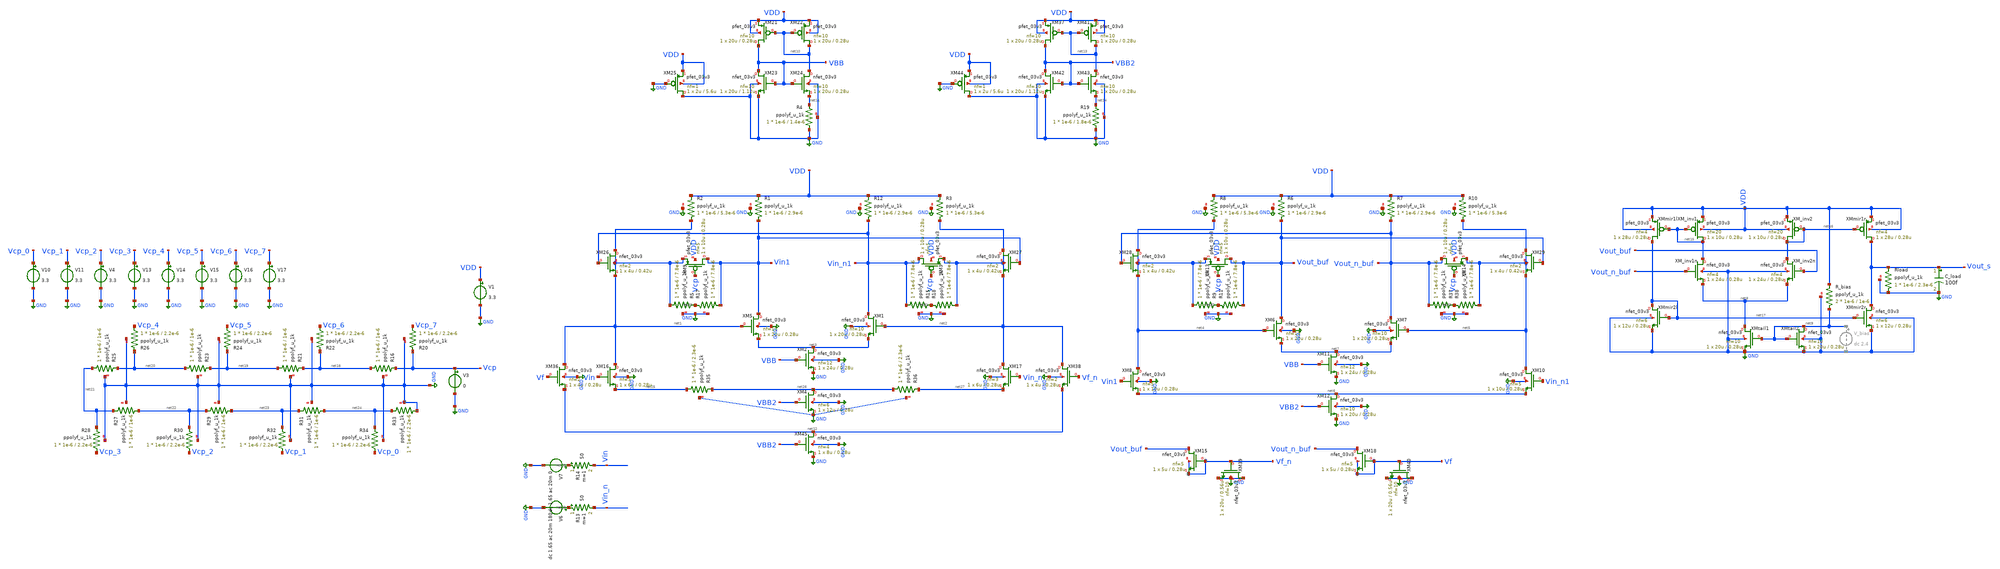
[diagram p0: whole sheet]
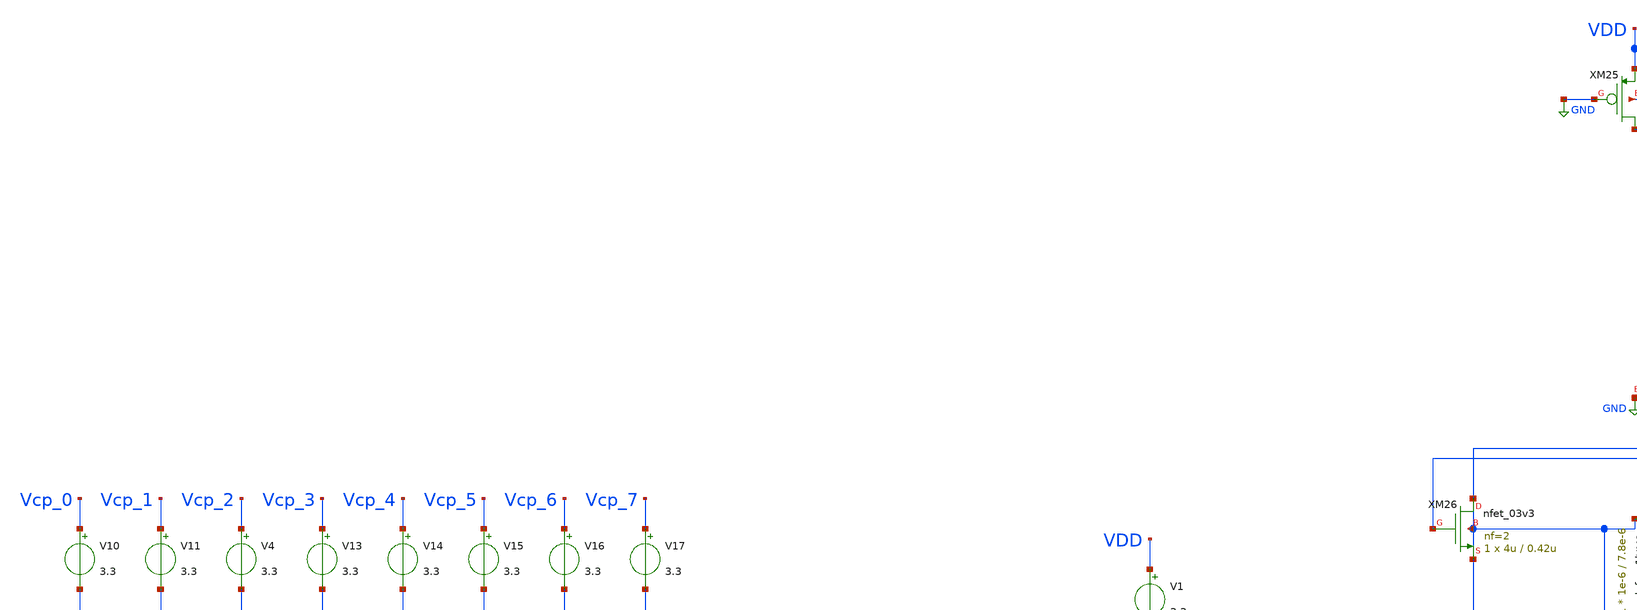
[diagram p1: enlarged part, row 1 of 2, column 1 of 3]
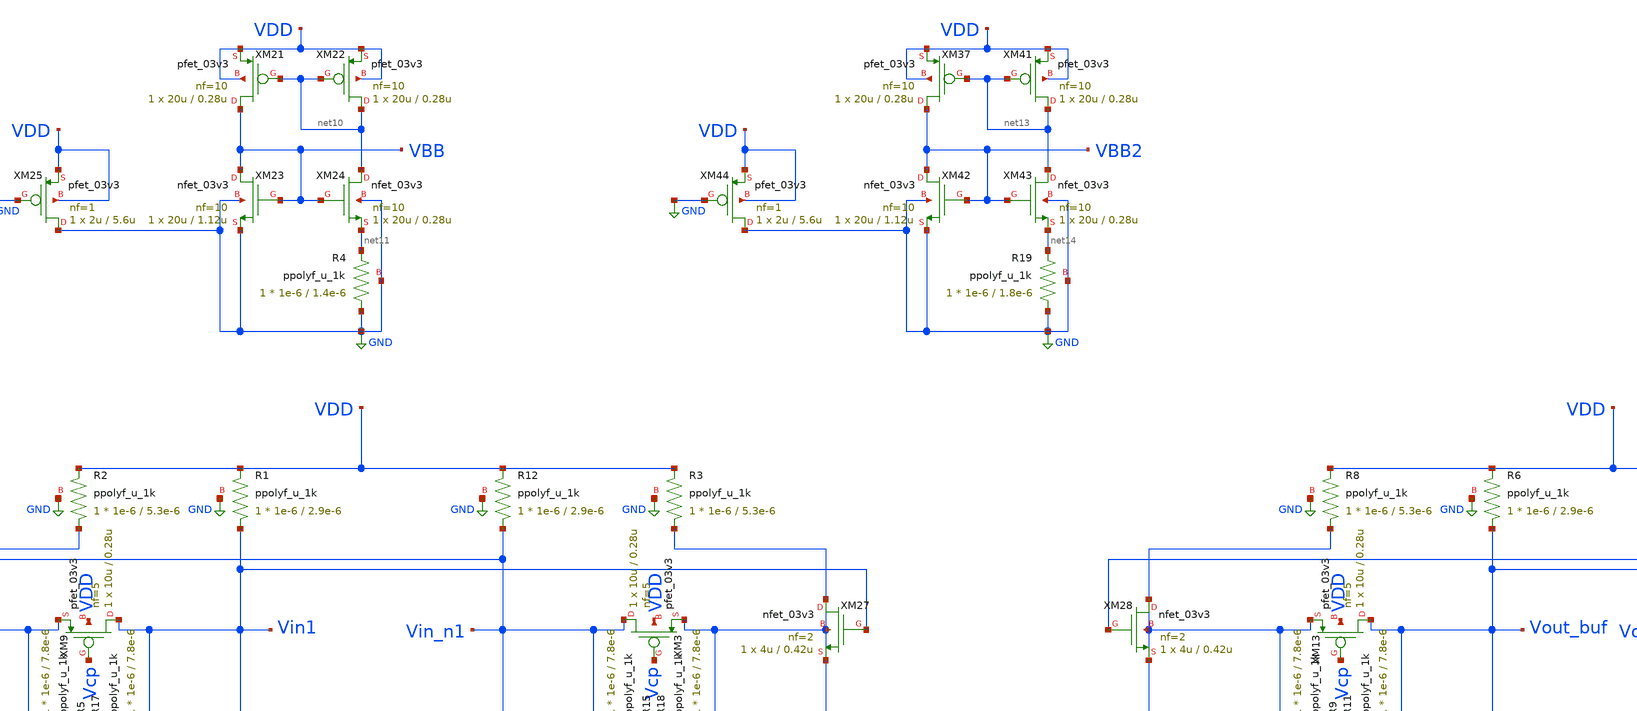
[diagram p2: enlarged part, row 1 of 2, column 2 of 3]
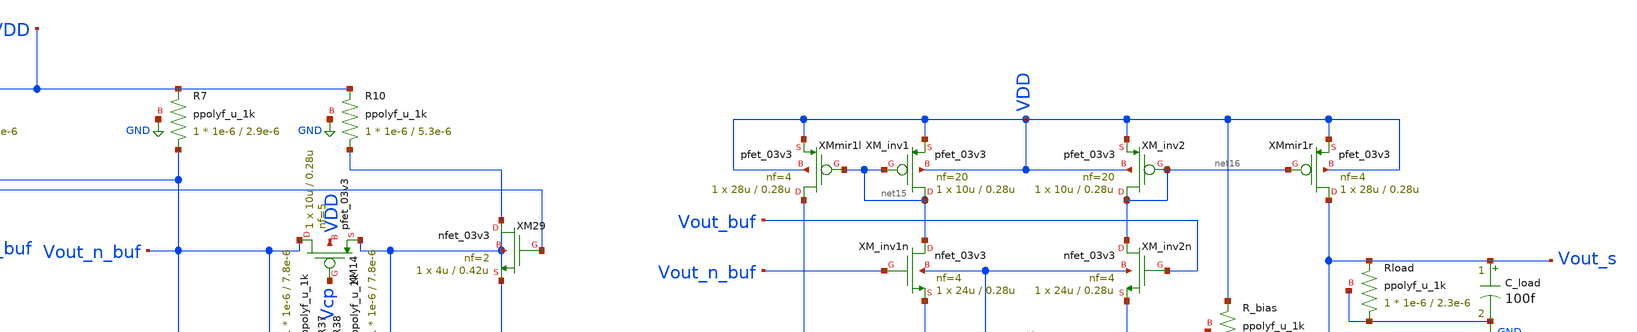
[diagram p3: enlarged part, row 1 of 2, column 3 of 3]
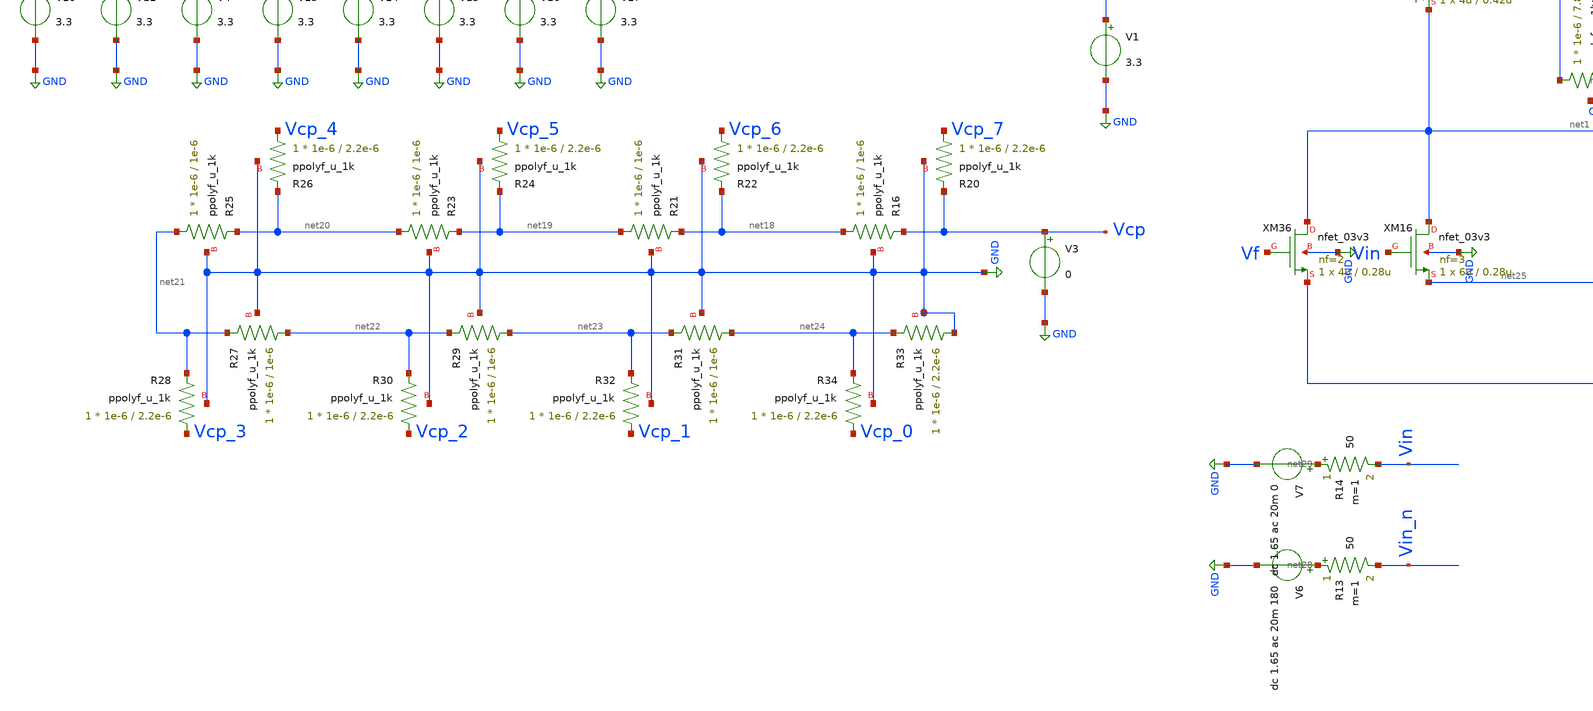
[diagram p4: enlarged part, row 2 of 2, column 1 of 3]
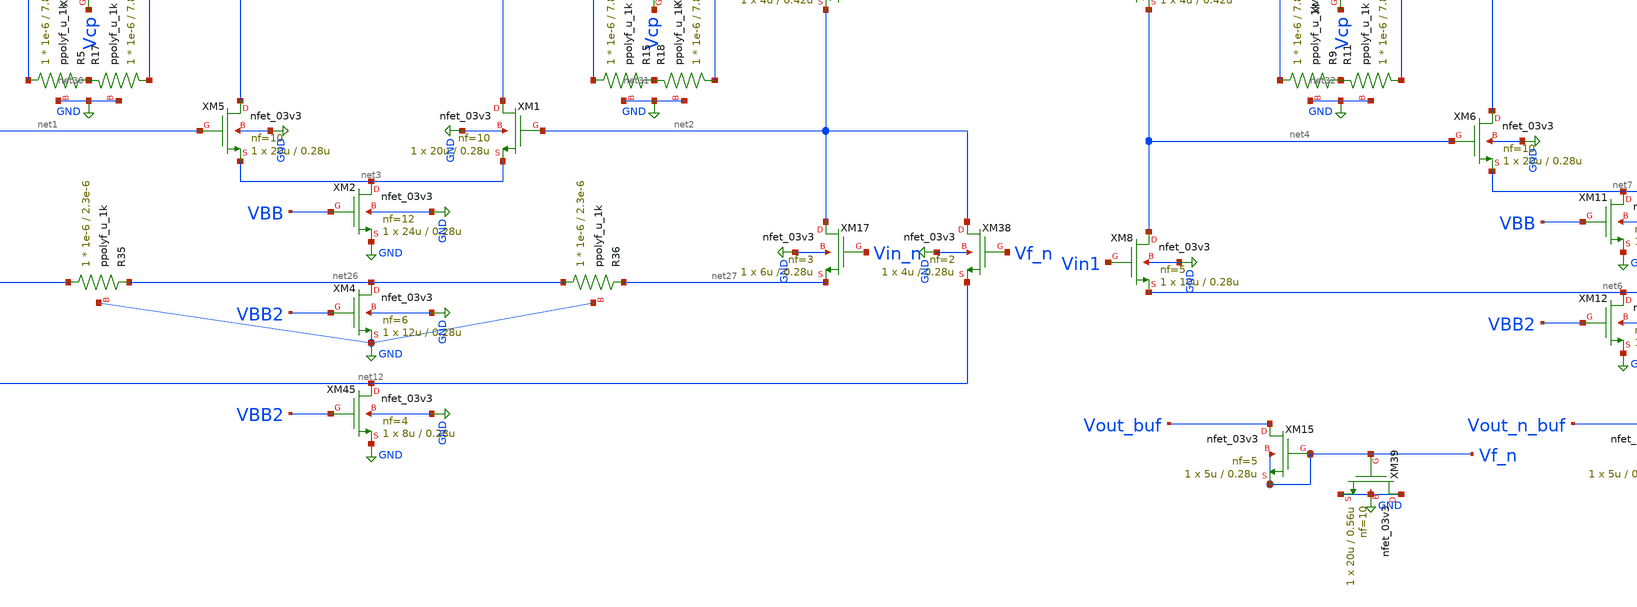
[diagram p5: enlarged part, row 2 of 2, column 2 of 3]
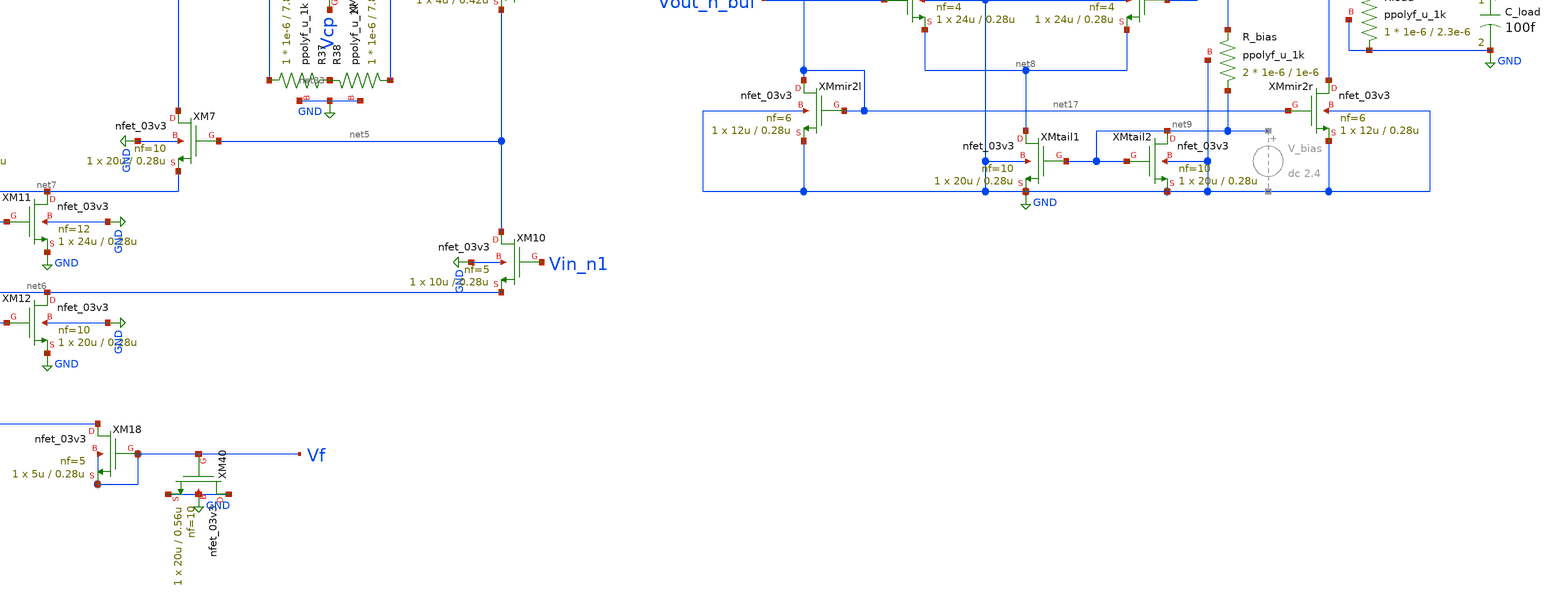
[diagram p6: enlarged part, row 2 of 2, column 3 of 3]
** sch_path: blocks/vga/vga.sch
**.subckt vga
V1 VDD GND 3.3
V6 net28 GND dc 1.65 ac 20m 180
XM5 Vin1 net1 net3 GND nfet_03v3 L=0.28u W=20u nf=10 ad='int((nf+1)/2) * W/nf * 0.18u' as='int((nf+2)/2) * W/nf * 0.18u'
+ pd='2*int((nf+1)/2) * (W/nf + 0.18u)' ps='2*int((nf+2)/2) * (W/nf + 0.18u)' nrd='0.18u / W' nrs='0.18u / W'
+ sa=0 sb=0 sd=0 m=1
XM1 Vin_n1 net2 net3 GND nfet_03v3 L=0.28u W=20u nf=10 ad='int((nf+1)/2) * W/nf * 0.18u' as='int((nf+2)/2) * W/nf * 0.18u'
+ pd='2*int((nf+1)/2) * (W/nf + 0.18u)' ps='2*int((nf+2)/2) * (W/nf + 0.18u)' nrd='0.18u / W' nrs='0.18u / W'
+ sa=0 sb=0 sd=0 m=1
XM16 net1 Vin net25 GND nfet_03v3 L=0.28u W=6u nf=3 ad='int((nf+1)/2) * W/nf * 0.18u' as='int((nf+2)/2) * W/nf * 0.18u'
+ pd='2*int((nf+1)/2) * (W/nf + 0.18u)' ps='2*int((nf+2)/2) * (W/nf + 0.18u)' nrd='0.18u / W' nrs='0.18u / W'
+ sa=0 sb=0 sd=0 m=1
XM17 net2 Vin_n net27 GND nfet_03v3 L=0.28u W=6u nf=3 ad='int((nf+1)/2) * W/nf * 0.18u' as='int((nf+2)/2) * W/nf * 0.18u'
+ pd='2*int((nf+1)/2) * (W/nf + 0.18u)' ps='2*int((nf+2)/2) * (W/nf + 0.18u)' nrd='0.18u / W' nrs='0.18u / W'
+ sa=0 sb=0 sd=0 m=1
XM2 net3 VBB GND GND nfet_03v3 L=0.28u W=24u nf=12 ad='int((nf+1)/2) * W/nf * 0.18u' as='int((nf+2)/2) * W/nf * 0.18u'
+ pd='2*int((nf+1)/2) * (W/nf + 0.18u)' ps='2*int((nf+2)/2) * (W/nf + 0.18u)' nrd='0.18u / W' nrs='0.18u / W'
+ sa=0 sb=0 sd=0 m=1
XM4 net26 VBB2 GND GND nfet_03v3 L=0.28u W=12u nf=6 ad='int((nf+1)/2) * W/nf * 0.18u' as='int((nf+2)/2) * W/nf * 0.18u'
+ pd='2*int((nf+1)/2) * (W/nf + 0.18u)' ps='2*int((nf+2)/2) * (W/nf + 0.18u)' nrd='0.18u / W' nrs='0.18u / W'
+ sa=0 sb=0 sd=0 m=1
XM9 Vin1 Vcp net1 VDD pfet_03v3 L=0.28u W=10u nf=5 ad='int((nf+1)/2) * W/nf * 0.18u' as='int((nf+2)/2) * W/nf * 0.18u'
+ pd='2*int((nf+1)/2) * (W/nf + 0.18u)' ps='2*int((nf+2)/2) * (W/nf + 0.18u)' nrd='0.18u / W' nrs='0.18u / W'
+ sa=0 sb=0 sd=0 m=1
XM6 Vout_buf net4 net7 GND nfet_03v3 L=0.28u W=20u nf=10 ad='int((nf+1)/2) * W/nf * 0.18u' as='int((nf+2)/2) * W/nf * 0.18u'
+ pd='2*int((nf+1)/2) * (W/nf + 0.18u)' ps='2*int((nf+2)/2) * (W/nf + 0.18u)' nrd='0.18u / W' nrs='0.18u / W'
+ sa=0 sb=0 sd=0 m=1
XM7 Vout_n_buf net5 net7 GND nfet_03v3 L=0.28u W=20u nf=10 ad='int((nf+1)/2) * W/nf * 0.18u' as='int((nf+2)/2) * W/nf * 0.18u'
+ pd='2*int((nf+1)/2) * (W/nf + 0.18u)' ps='2*int((nf+2)/2) * (W/nf + 0.18u)' nrd='0.18u / W' nrs='0.18u / W'
+ sa=0 sb=0 sd=0 m=1
XM8 net4 Vin1 net6 GND nfet_03v3 L=0.28u W=10u nf=5 ad='int((nf+1)/2) * W/nf * 0.18u' as='int((nf+2)/2) * W/nf * 0.18u'
+ pd='2*int((nf+1)/2) * (W/nf + 0.18u)' ps='2*int((nf+2)/2) * (W/nf + 0.18u)' nrd='0.18u / W' nrs='0.18u / W'
+ sa=0 sb=0 sd=0 m=1
XM10 net5 Vin_n1 net6 GND nfet_03v3 L=0.28u W=10u nf=5 ad='int((nf+1)/2) * W/nf * 0.18u' as='int((nf+2)/2) * W/nf * 0.18u'
+ pd='2*int((nf+1)/2) * (W/nf + 0.18u)' ps='2*int((nf+2)/2) * (W/nf + 0.18u)' nrd='0.18u / W' nrs='0.18u / W'
+ sa=0 sb=0 sd=0 m=1
XM11 net7 VBB GND GND nfet_03v3 L=0.28u W=24u nf=12 ad='int((nf+1)/2) * W/nf * 0.18u' as='int((nf+2)/2) * W/nf * 0.18u'
+ pd='2*int((nf+1)/2) * (W/nf + 0.18u)' ps='2*int((nf+2)/2) * (W/nf + 0.18u)' nrd='0.18u / W' nrs='0.18u / W'
+ sa=0 sb=0 sd=0 m=1
XM12 net6 VBB2 GND GND nfet_03v3 L=0.28u W=20u nf=10 ad='int((nf+1)/2) * W/nf * 0.18u' as='int((nf+2)/2) * W/nf * 0.18u'
+ pd='2*int((nf+1)/2) * (W/nf + 0.18u)' ps='2*int((nf+2)/2) * (W/nf + 0.18u)' nrd='0.18u / W' nrs='0.18u / W'
+ sa=0 sb=0 sd=0 m=1
V7 net29 GND dc 1.65 ac 20m 0
R14 net29 Vin 50 m=1
R13 net28 Vin_n 50 m=1
XM21 VBB net10 VDD VDD pfet_03v3 L=0.28u W=20u nf=10 ad='int((nf+1)/2) * W/nf * 0.18u' as='int((nf+2)/2) * W/nf * 0.18u'
+ pd='2*int((nf+1)/2) * (W/nf + 0.18u)' ps='2*int((nf+2)/2) * (W/nf + 0.18u)' nrd='0.18u / W' nrs='0.18u / W'
+ sa=0 sb=0 sd=0 m=1
XM22 net10 net10 VDD VDD pfet_03v3 L=0.28u W=20u nf=10 ad='int((nf+1)/2) * W/nf * 0.18u' as='int((nf+2)/2) * W/nf * 0.18u'
+ pd='2*int((nf+1)/2) * (W/nf + 0.18u)' ps='2*int((nf+2)/2) * (W/nf + 0.18u)' nrd='0.18u / W' nrs='0.18u / W'
+ sa=0 sb=0 sd=0 m=1
XM23 VBB VBB GND GND nfet_03v3 L=1.12u W=20u nf=10 ad='int((nf+1)/2) * W/nf * 0.18u' as='int((nf+2)/2) * W/nf * 0.18u'
+ pd='2*int((nf+1)/2) * (W/nf + 0.18u)' ps='2*int((nf+2)/2) * (W/nf + 0.18u)' nrd='0.18u / W' nrs='0.18u / W'
+ sa=0 sb=0 sd=0 m=1
XM24 net10 VBB net11 GND nfet_03v3 L=0.28u W=20u nf=10 ad='int((nf+1)/2) * W/nf * 0.18u' as='int((nf+2)/2) * W/nf * 0.18u'
+ pd='2*int((nf+1)/2) * (W/nf + 0.18u)' ps='2*int((nf+2)/2) * (W/nf + 0.18u)' nrd='0.18u / W' nrs='0.18u / W'
+ sa=0 sb=0 sd=0 m=1
XM25 GND GND VDD VDD pfet_03v3 L=5.6u W=2u nf=1 ad='int((nf+1)/2) * W/nf * 0.18u' as='int((nf+2)/2) * W/nf * 0.18u'
+ pd='2*int((nf+1)/2) * (W/nf + 0.18u)' ps='2*int((nf+2)/2) * (W/nf + 0.18u)' nrd='0.18u / W' nrs='0.18u / W'
+ sa=0 sb=0 sd=0 m=1
XR4 GND net11 GND ppolyf_u_1k r_width=1e-6 r_length=1.4e-6 m=1
XM26 net1 Vin_n1 net1 net1 nfet_03v3 L=0.42u W=4u nf=2 ad='int((nf+1)/2) * W/nf * 0.18u' as='int((nf+2)/2) * W/nf * 0.18u'
+ pd='2*int((nf+1)/2) * (W/nf + 0.18u)' ps='2*int((nf+2)/2) * (W/nf + 0.18u)' nrd='0.18u / W' nrs='0.18u / W'
+ sa=0 sb=0 sd=0 m=1
XM27 net2 Vin1 net2 net2 nfet_03v3 L=0.42u W=4u nf=2 ad='int((nf+1)/2) * W/nf * 0.18u' as='int((nf+2)/2) * W/nf * 0.18u'
+ pd='2*int((nf+1)/2) * (W/nf + 0.18u)' ps='2*int((nf+2)/2) * (W/nf + 0.18u)' nrd='0.18u / W' nrs='0.18u / W'
+ sa=0 sb=0 sd=0 m=1
XM28 net4 Vout_n_buf net4 net4 nfet_03v3 L=0.42u W=4u nf=2 ad='int((nf+1)/2) * W/nf * 0.18u' as='int((nf+2)/2) * W/nf * 0.18u'
+ pd='2*int((nf+1)/2) * (W/nf + 0.18u)' ps='2*int((nf+2)/2) * (W/nf + 0.18u)' nrd='0.18u / W' nrs='0.18u / W'
+ sa=0 sb=0 sd=0 m=1
XM29 net5 Vout_buf net5 net5 nfet_03v3 L=0.42u W=4u nf=2 ad='int((nf+1)/2) * W/nf * 0.18u' as='int((nf+2)/2) * W/nf * 0.18u'
+ pd='2*int((nf+1)/2) * (W/nf + 0.18u)' ps='2*int((nf+2)/2) * (W/nf + 0.18u)' nrd='0.18u / W' nrs='0.18u / W'
+ sa=0 sb=0 sd=0 m=1
XM_inv1 net15 net15 VDD VDD pfet_03v3 L=0.28u W=10u nf=20 ad='int((nf+1)/2) * W/nf * 0.18u' as='int((nf+2)/2) * W/nf * 0.18u'
+ pd='2*int((nf+1)/2) * (W/nf + 0.18u)' ps='2*int((nf+2)/2) * (W/nf + 0.18u)' nrd='0.18u / W' nrs='0.18u / W'
+ sa=0 sb=0 sd=0 m=1
XM_inv1n net15 Vout_n_buf net8 GND nfet_03v3 L=0.28u W=24u nf=4 ad='int((nf+1)/2) * W/nf * 0.18u' as='int((nf+2)/2) * W/nf * 0.18u'
+ pd='2*int((nf+1)/2) * (W/nf + 0.18u)' ps='2*int((nf+2)/2) * (W/nf + 0.18u)' nrd='0.18u / W' nrs='0.18u / W'
+ sa=0 sb=0 sd=0 m=1
XM_inv2 net16 net16 VDD VDD pfet_03v3 L=0.28u W=10u nf=20 ad='int((nf+1)/2) * W/nf * 0.18u' as='int((nf+2)/2) * W/nf * 0.18u'
+ pd='2*int((nf+1)/2) * (W/nf + 0.18u)' ps='2*int((nf+2)/2) * (W/nf + 0.18u)' nrd='0.18u / W' nrs='0.18u / W'
+ sa=0 sb=0 sd=0 m=1
XM_inv2n net16 Vout_buf net8 GND nfet_03v3 L=0.28u W=24u nf=4 ad='int((nf+1)/2) * W/nf * 0.18u' as='int((nf+2)/2) * W/nf * 0.18u'
+ pd='2*int((nf+1)/2) * (W/nf + 0.18u)' ps='2*int((nf+2)/2) * (W/nf + 0.18u)' nrd='0.18u / W' nrs='0.18u / W'
+ sa=0 sb=0 sd=0 m=1
XMtail1 net8 net9 GND GND nfet_03v3 L=0.28u W=20u nf=10 ad='int((nf+1)/2) * W/nf * 0.18u' as='int((nf+2)/2) * W/nf * 0.18u'
+ pd='2*int((nf+1)/2) * (W/nf + 0.18u)' ps='2*int((nf+2)/2) * (W/nf + 0.18u)' nrd='0.18u / W' nrs='0.18u / W'
+ sa=0 sb=0 sd=0 m=1
XMtail2 net9 net9 GND GND nfet_03v3 L=0.28u W=20u nf=10 ad='int((nf+1)/2) * W/nf * 0.18u' as='int((nf+2)/2) * W/nf * 0.18u'
+ pd='2*int((nf+1)/2) * (W/nf + 0.18u)' ps='2*int((nf+2)/2) * (W/nf + 0.18u)' nrd='0.18u / W' nrs='0.18u / W'
+ sa=0 sb=0 sd=0 m=1
XM36 net1 Vf net12 GND nfet_03v3 L=0.28u W=4u nf=2 ad='int((nf+1)/2) * W/nf * 0.18u' as='int((nf+2)/2) * W/nf * 0.18u'
+ pd='2*int((nf+1)/2) * (W/nf + 0.18u)' ps='2*int((nf+2)/2) * (W/nf + 0.18u)' nrd='0.18u / W' nrs='0.18u / W'
+ sa=0 sb=0 sd=0 m=1
XM38 net2 Vf_n net12 GND nfet_03v3 L=0.28u W=4u nf=2 ad='int((nf+1)/2) * W/nf * 0.18u' as='int((nf+2)/2) * W/nf * 0.18u'
+ pd='2*int((nf+1)/2) * (W/nf + 0.18u)' ps='2*int((nf+2)/2) * (W/nf + 0.18u)' nrd='0.18u / W' nrs='0.18u / W'
+ sa=0 sb=0 sd=0 m=1
XM39 GND Vf_n GND GND nfet_03v3 L=0.56u W=20u nf=10 ad='int((nf+1)/2) * W/nf * 0.18u' as='int((nf+2)/2) * W/nf * 0.18u'
+ pd='2*int((nf+1)/2) * (W/nf + 0.18u)' ps='2*int((nf+2)/2) * (W/nf + 0.18u)' nrd='0.18u / W' nrs='0.18u / W'
+ sa=0 sb=0 sd=0 m=1
XM40 GND Vf GND GND nfet_03v3 L=0.56u W=20u nf=10 ad='int((nf+1)/2) * W/nf * 0.18u' as='int((nf+2)/2) * W/nf * 0.18u'
+ pd='2*int((nf+1)/2) * (W/nf + 0.18u)' ps='2*int((nf+2)/2) * (W/nf + 0.18u)' nrd='0.18u / W' nrs='0.18u / W'
+ sa=0 sb=0 sd=0 m=1
XM37 VBB2 net13 VDD VDD pfet_03v3 L=0.28u W=20u nf=10 ad='int((nf+1)/2) * W/nf * 0.18u' as='int((nf+2)/2) * W/nf * 0.18u'
+ pd='2*int((nf+1)/2) * (W/nf + 0.18u)' ps='2*int((nf+2)/2) * (W/nf + 0.18u)' nrd='0.18u / W' nrs='0.18u / W'
+ sa=0 sb=0 sd=0 m=1
XM41 net13 net13 VDD VDD pfet_03v3 L=0.28u W=20u nf=10 ad='int((nf+1)/2) * W/nf * 0.18u' as='int((nf+2)/2) * W/nf * 0.18u'
+ pd='2*int((nf+1)/2) * (W/nf + 0.18u)' ps='2*int((nf+2)/2) * (W/nf + 0.18u)' nrd='0.18u / W' nrs='0.18u / W'
+ sa=0 sb=0 sd=0 m=1
XM42 VBB2 VBB2 GND GND nfet_03v3 L=1.12u W=20u nf=10 ad='int((nf+1)/2) * W/nf * 0.18u' as='int((nf+2)/2) * W/nf * 0.18u'
+ pd='2*int((nf+1)/2) * (W/nf + 0.18u)' ps='2*int((nf+2)/2) * (W/nf + 0.18u)' nrd='0.18u / W' nrs='0.18u / W'
+ sa=0 sb=0 sd=0 m=1
XM43 net13 VBB2 net14 GND nfet_03v3 L=0.28u W=20u nf=10 ad='int((nf+1)/2) * W/nf * 0.18u' as='int((nf+2)/2) * W/nf * 0.18u'
+ pd='2*int((nf+1)/2) * (W/nf + 0.18u)' ps='2*int((nf+2)/2) * (W/nf + 0.18u)' nrd='0.18u / W' nrs='0.18u / W'
+ sa=0 sb=0 sd=0 m=1
XM44 GND GND VDD VDD pfet_03v3 L=5.6u W=2u nf=1 ad='int((nf+1)/2) * W/nf * 0.18u' as='int((nf+2)/2) * W/nf * 0.18u'
+ pd='2*int((nf+1)/2) * (W/nf + 0.18u)' ps='2*int((nf+2)/2) * (W/nf + 0.18u)' nrd='0.18u / W' nrs='0.18u / W'
+ sa=0 sb=0 sd=0 m=1
XR19 GND net14 GND ppolyf_u_1k r_width=1e-6 r_length=1.8e-6 m=1
XM45 net12 VBB2 GND GND nfet_03v3 L=0.28u W=8u nf=4 ad='int((nf+1)/2) * W/nf * 0.18u' as='int((nf+2)/2) * W/nf * 0.18u'
+ pd='2*int((nf+1)/2) * (W/nf + 0.18u)' ps='2*int((nf+2)/2) * (W/nf + 0.18u)' nrd='0.18u / W' nrs='0.18u / W'
+ sa=0 sb=0 sd=0 m=1
XMmir1l net17 net15 VDD VDD pfet_03v3 L=0.28u W=28u nf=4 ad='int((nf+1)/2) * W/nf * 0.18u' as='int((nf+2)/2) * W/nf * 0.18u'
+ pd='2*int((nf+1)/2) * (W/nf + 0.18u)' ps='2*int((nf+2)/2) * (W/nf + 0.18u)' nrd='0.18u / W' nrs='0.18u / W'
+ sa=0 sb=0 sd=0 m=1
XMmir1r Vout_s net16 VDD VDD pfet_03v3 L=0.28u W=28u nf=4 ad='int((nf+1)/2) * W/nf * 0.18u' as='int((nf+2)/2) * W/nf * 0.18u'
+ pd='2*int((nf+1)/2) * (W/nf + 0.18u)' ps='2*int((nf+2)/2) * (W/nf + 0.18u)' nrd='0.18u / W' nrs='0.18u / W'
+ sa=0 sb=0 sd=0 m=1
XMmir2l net17 net17 GND GND nfet_03v3 L=0.28u W=12u nf=6 ad='int((nf+1)/2) * W/nf * 0.18u' as='int((nf+2)/2) * W/nf * 0.18u'
+ pd='2*int((nf+1)/2) * (W/nf + 0.18u)' ps='2*int((nf+2)/2) * (W/nf + 0.18u)' nrd='0.18u / W' nrs='0.18u / W'
+ sa=0 sb=0 sd=0 m=1
XMmir2r Vout_s net17 GND GND nfet_03v3 L=0.28u W=12u nf=6 ad='int((nf+1)/2) * W/nf * 0.18u' as='int((nf+2)/2) * W/nf * 0.18u'
+ pd='2*int((nf+1)/2) * (W/nf + 0.18u)' ps='2*int((nf+2)/2) * (W/nf + 0.18u)' nrd='0.18u / W' nrs='0.18u / W'
+ sa=0 sb=0 sd=0 m=1
XR_bias net9 VDD GND ppolyf_u_1k r_width=1e-6 r_length=1e-6 m=2
C_load Vout_s GND 100f m=1
XR16 net18 Vcp GND ppolyf_u_1k r_width=1e-6 r_length=1e-6 m=1
XR20 Vcp_7 Vcp GND ppolyf_u_1k r_width=1e-6 r_length=2.2e-6 m=1
XR21 net19 net18 GND ppolyf_u_1k r_width=1e-6 r_length=1e-6 m=1
XR22 Vcp_6 net18 GND ppolyf_u_1k r_width=1e-6 r_length=2.2e-6 m=1
XR23 net20 net19 GND ppolyf_u_1k r_width=1e-6 r_length=1e-6 m=1
XR24 Vcp_5 net19 GND ppolyf_u_1k r_width=1e-6 r_length=2.2e-6 m=1
XR25 net21 net20 GND ppolyf_u_1k r_width=1e-6 r_length=1e-6 m=1
XR26 Vcp_4 net20 GND ppolyf_u_1k r_width=1e-6 r_length=2.2e-6 m=1
XR27 net22 net21 GND ppolyf_u_1k r_width=1e-6 r_length=1e-6 m=1
XR28 Vcp_3 net21 GND ppolyf_u_1k r_width=1e-6 r_length=2.2e-6 m=1
XR29 net23 net22 GND ppolyf_u_1k r_width=1e-6 r_length=1e-6 m=1
XR30 Vcp_2 net22 GND ppolyf_u_1k r_width=1e-6 r_length=2.2e-6 m=1
XR31 net24 net23 GND ppolyf_u_1k r_width=1e-6 r_length=1e-6 m=1
XR32 Vcp_1 net23 GND ppolyf_u_1k r_width=1e-6 r_length=2.2e-6 m=1
XR33 GND net24 GND ppolyf_u_1k r_width=1e-6 r_length=2.2e-6 m=1
XR34 Vcp_0 net24 GND ppolyf_u_1k r_width=1e-6 r_length=2.2e-6 m=1
V10 Vcp_0 GND 3.3
V11 Vcp_1 GND 3.3
V4 Vcp_2 GND 3.3
V13 Vcp_3 GND 3.3
V14 Vcp_4 GND 3.3
V15 Vcp_5 GND 3.3
V16 Vcp_6 GND 3.3
V17 Vcp_7 GND 3.3
V3 Vcp GND 0
XR35 net25 net26 GND ppolyf_u_1k r_width=1e-6 r_length=2.3e-6 m=1
XR36 net26 net27 GND ppolyf_u_1k r_width=1e-6 r_length=2.3e-6 m=1
XM15 Vout_buf Vf_n Vf_n Vf_n nfet_03v3 L=0.28u W=5u nf=5 ad='int((nf+1)/2) * W/nf * 0.18u' as='int((nf+2)/2) * W/nf * 0.18u'
+ pd='2*int((nf+1)/2) * (W/nf + 0.18u)' ps='2*int((nf+2)/2) * (W/nf + 0.18u)' nrd='0.18u / W' nrs='0.18u / W'
+ sa=0 sb=0 sd=0 m=1
XM18 Vout_n_buf Vf Vf Vf nfet_03v3 L=0.28u W=5u nf=5 ad='int((nf+1)/2) * W/nf * 0.18u' as='int((nf+2)/2) * W/nf * 0.18u'
+ pd='2*int((nf+1)/2) * (W/nf + 0.18u)' ps='2*int((nf+2)/2) * (W/nf + 0.18u)' nrd='0.18u / W' nrs='0.18u / W'
+ sa=0 sb=0 sd=0 m=1
XR5 net1 net30 GND ppolyf_u_1k r_width=1e-6 r_length=7.8e-6 m=1
XR17 Vin1 net30 GND ppolyf_u_1k r_width=1e-6 r_length=7.8e-6 m=1
XM3 Vin_n1 Vcp net2 VDD pfet_03v3 L=0.28u W=10u nf=5 ad='int((nf+1)/2) * W/nf * 0.18u' as='int((nf+2)/2) * W/nf * 0.18u'
+ pd='2*int((nf+1)/2) * (W/nf + 0.18u)' ps='2*int((nf+2)/2) * (W/nf + 0.18u)' nrd='0.18u / W' nrs='0.18u / W'
+ sa=0 sb=0 sd=0 m=1
XR15 Vin_n1 net31 GND ppolyf_u_1k r_width=1e-6 r_length=7.8e-6 m=1
XR18 net2 net31 GND ppolyf_u_1k r_width=1e-6 r_length=7.8e-6 m=1
XM13 Vout_buf Vcp net4 VDD pfet_03v3 L=0.28u W=10u nf=5 ad='int((nf+1)/2) * W/nf * 0.18u' as='int((nf+2)/2) * W/nf * 0.18u'
+ pd='2*int((nf+1)/2) * (W/nf + 0.18u)' ps='2*int((nf+2)/2) * (W/nf + 0.18u)' nrd='0.18u / W' nrs='0.18u / W'
+ sa=0 sb=0 sd=0 m=1
XR9 net4 net32 GND ppolyf_u_1k r_width=1e-6 r_length=7.8e-6 m=1
XR11 Vout_buf net32 GND ppolyf_u_1k r_width=1e-6 r_length=7.8e-6 m=1
XM14 Vout_n_buf Vcp net5 VDD pfet_03v3 L=0.28u W=10u nf=5 ad='int((nf+1)/2) * W/nf * 0.18u' as='int((nf+2)/2) * W/nf * 0.18u'
+ pd='2*int((nf+1)/2) * (W/nf + 0.18u)' ps='2*int((nf+2)/2) * (W/nf + 0.18u)' nrd='0.18u / W' nrs='0.18u / W'
+ sa=0 sb=0 sd=0 m=1
XR37 Vout_n_buf net33 GND ppolyf_u_1k r_width=1e-6 r_length=7.8e-6 m=1
XR38 net5 net33 GND ppolyf_u_1k r_width=1e-6 r_length=7.8e-6 m=1
XRload GND Vout_s GND ppolyf_u_1k r_width=1e-6 r_length=2.3e-6 m=1
XR1 Vin1 VDD GND ppolyf_u_1k r_width=1e-6 r_length=2.9e-6 m=1
XR12 Vin_n1 VDD GND ppolyf_u_1k r_width=1e-6 r_length=2.9e-6 m=1
XR6 Vout_buf VDD GND ppolyf_u_1k r_width=1e-6 r_length=2.9e-6 m=1
XR7 Vout_n_buf VDD GND ppolyf_u_1k r_width=1e-6 r_length=2.9e-6 m=1
XR3 net2 VDD GND ppolyf_u_1k r_width=1e-6 r_length=5.3e-6 m=1
XR2 net1 VDD GND ppolyf_u_1k r_width=1e-6 r_length=5.3e-6 m=1
XR8 net4 VDD GND ppolyf_u_1k r_width=1e-6 r_length=5.3e-6 m=1
XR10 net5 VDD GND ppolyf_u_1k r_width=1e-6 r_length=5.3e-6 m=1
**** begin user architecture code


.include /foss/pdks/gf180mcuD/libs.tech/ngspice/design.ngspice
.lib /foss/pdks/gf180mcuD/libs.tech/ngspice/sm141064.ngspice typical
.lib /foss/pdks/gf180mcuD/libs.tech/ngspice/sm141064.ngspice bjt_typical
.lib /foss/pdks/gf180mcuD/libs.tech/ngspice/sm141064.ngspice diode_typical
.lib /foss/pdks/gf180mcuD/libs.tech/ngspice/sm141064.ngspice res_typical
.lib /foss/pdks/gf180mcuD/libs.tech/ngspice/sm141064.ngspice mimcap_typical
.lib /foss/pdks/gf180mcuD/libs.tech/ngspice/sm141064.ngspice moscap_typical
.option method=gear

.control
set temp = 25
  * 1. Setup the sweep parameters
  let v_ctrl = 0.6

  let f_start = 1
  let f_stop = 3.2G
  let f_points = 120

  * 2. Initialize vectors to store results
  let gain_db = unitvec(f_points)

  alter v3 = v_ctrl
  ac dec $&f_points $&f_start $&f_stop

  * 4. Calculate Differential Gain in dB
  * Formula: 20 * log10(|Vout_diff| / |Vin_diff|)
  let vin_mag = mag(v(vin) - v(vin_n))
  let vout_s_mag = mag(v(vout_s))
  let vout_buf_mag = mag(v(vout_buf) - v(vout_n_buf))
  let vout_s_gain = 20 * log10(vout_s_mag / vin_mag)
  let vout_buf_gain = 20 * log10(vout_buf_mag / vin_mag)

  * Credit to marcel hendrix
  * https://sourceforge.net/p/ngspice/discussion/133842/thread/2031ad61/
  meas ac peak  MAX  vmag(vout_s) FROM=$&f_start TO=$&f_stop
  let f3db = peak/sqrt(2)
  meas ac lo_3db WHEN vmag(vout_s)=f3db RISE=1
  meas ac hi_3db WHEN vmag(vout_s)=f3db FALL=1

  * 5. Save results to vectors
  plot vout_s_gain vout_buf_gain title 'Gain (dB) vs. Frequency from 1MHz to 3.2GHz, 0.6 vctrl' ylimit
+ 0 80
.endc


**** end user architecture code
**.ends
.GLOBAL GND
.end
